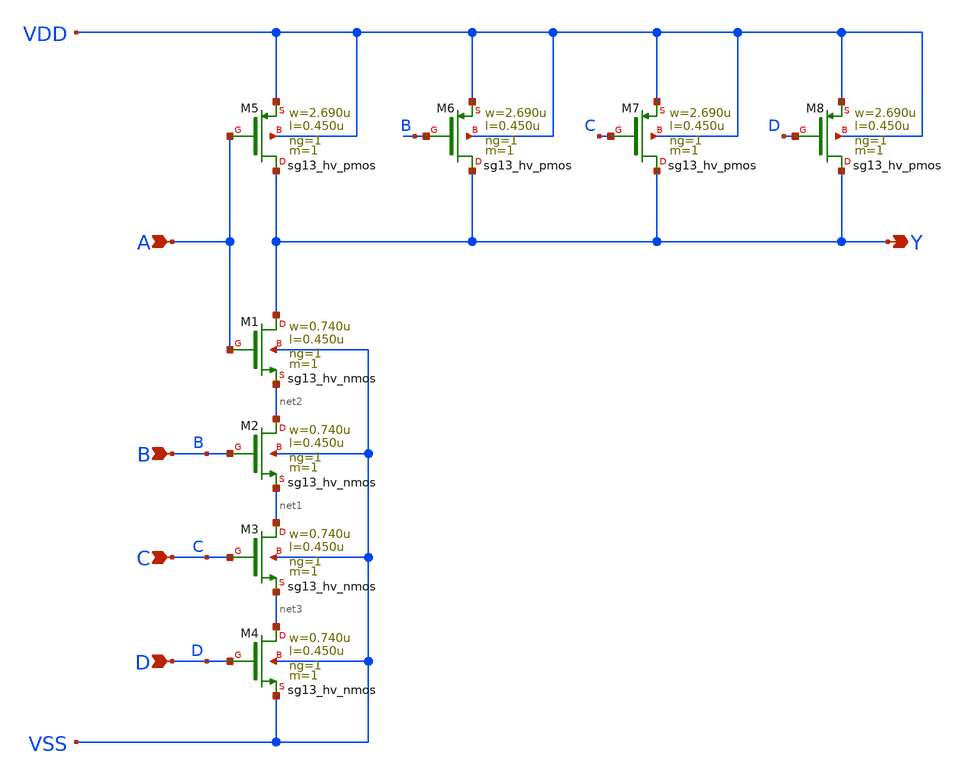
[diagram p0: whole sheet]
** sch_path: ihp-sg13g2/libs.ref/sg13g2_stdcell_hv/sch/xschem/sg13g2_hv_nand4_1.sch
* Copyright 2023 IHP PDK Authors
* Licensed under the Apache License, Version 2.0 (the "License");
* you may not use this file except in compliance with the License.
* You may obtain a copy of the License at
* https://www.apache.org/licenses/LICENSE-2.0
* Unless required by applicable law or agreed to in writing, software
* distributed under the License is distributed on an "AS IS" BASIS,
* WITHOUT WARRANTIES OR CONDITIONS OF ANY KIND, either express or implied.
* See the License for the specific language governing permissions and
* limitations under the License.
**.subckt sg13g2_hv_nand4_1 A B C Y D
*.ipin A
*.ipin B
*.ipin C
*.opin Y
*.ipin D
XM1 Y A net2 VSS sg13_hv_nmos w=0.740u l=0.450u ng=1 m=1 mm_ok=1
XM2 net2 B net1 VSS sg13_hv_nmos w=0.740u l=0.450u ng=1 m=1 mm_ok=1
XM3 net1 C net3 VSS sg13_hv_nmos w=0.740u l=0.450u ng=1 m=1 mm_ok=1
XM4 net3 D VSS VSS sg13_hv_nmos w=0.740u l=0.450u ng=1 m=1 mm_ok=1
XM5 Y A VDD VDD sg13_hv_pmos w=2.690u l=0.450u ng=1 m=1 mm_ok=1
XM6 Y B VDD VDD sg13_hv_pmos w=2.690u l=0.450u ng=1 m=1 mm_ok=1
XM7 Y C VDD VDD sg13_hv_pmos w=2.690u l=0.450u ng=1 m=1 mm_ok=1
XM8 Y D VDD VDD sg13_hv_pmos w=2.690u l=0.450u ng=1 m=1 mm_ok=1
**.ends
.end
